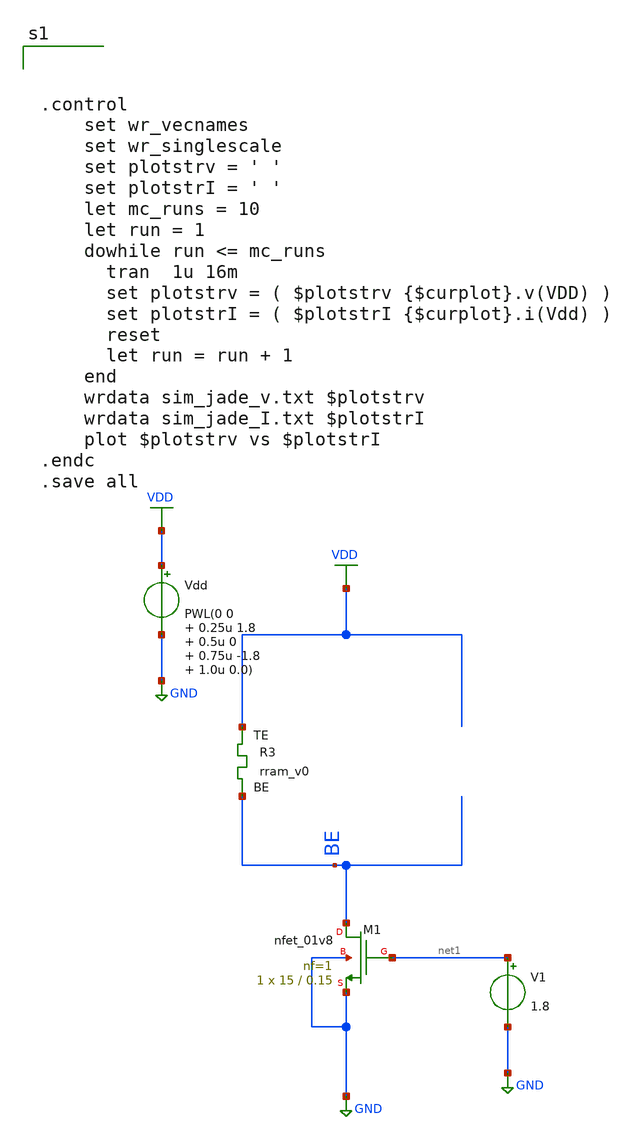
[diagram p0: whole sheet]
** sch_path: mc_mem.sch
**.subckt mc_mem
Vdd VDD GND PWL(0 0 0.25u 1.8 0.5u 0 0.75u -1.8 1.0u 0.0)
XR3 VDD BE rram_v0
XM1 BE net1 GND GND sky130_fd_pr__nfet_01v8 L=0.15 W=15 nf=1 ad='int((nf+1)/2) * W/nf * 0.29' as='int((nf+2)/2) * W/nf * 0.29'
+ pd='2*int((nf+1)/2) * (W/nf + 0.29)' ps='2*int((nf+2)/2) * (W/nf + 0.29)' nrd='0.29 / W' nrs='0.29 / W'
+ sa=0 sb=0 sd=0 mult=1 m=1
V1 net1 GND 1.8
**** begin user architecture code



.control
	set wr_vecnames
	set wr_singlescale
	set plotstrv = ' '
	set plotstrI = ' '
	let mc_runs = 10
	let run = 1
	dowhile run <= mc_runs
	  tran  1u 16m
	  set plotstrv = ( $plotstrv {$curplot}.v(VDD) )
	  set plotstrI = ( $plotstrI {$curplot}.i(Vdd) )
	  reset
	  let run = run + 1
	end
	wrdata sim_jade_v.txt $plotstrv
	wrdata sim_jade_I.txt $plotstrI
	plot $plotstrv vs $plotstrI
.endc
.save all




** opencircuitdesign pdks install
.inc $::SKYWATER_MODELS/rram_v0.spice


** opencircuitdesign pdks install
.param mc_tran=1.0
.lib $::SKYWATER_MODELS/sky130.lib.spice tt_mm


**** end user architecture code
**.ends
.GLOBAL GND
.GLOBAL VDD
.end
